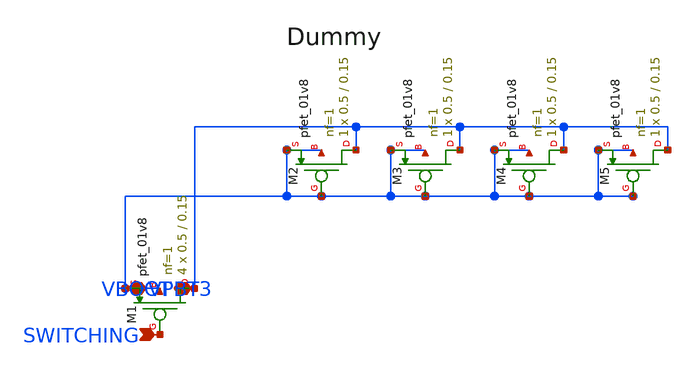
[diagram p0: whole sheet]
** sch_path: xschem/pcell_bsw_dischrg.sch
**.subckt pcell_bsw_dischrg VPBT3 SWITCHING VBOOT
*.iopin VPBT3
*.ipin SWITCHING
*.iopin VBOOT
XM1 VBOOT SWITCHING VPBT3 VPBT3 sky130_fd_pr__pfet_01v8 L=0.15 W=0.5 nf=1 ad='int((nf+1)/2) * W/nf * 0.29'
+ as='int((nf+2)/2) * W/nf * 0.29' pd='2*int((nf+1)/2) * (W/nf + 0.29)' ps='2*int((nf+2)/2) * (W/nf + 0.29)'
+ nrd='0.29 / W' nrs='0.29 / W' sa=0 sb=0 sd=0 mult=4 m=4
XM2 VBOOT VPBT3 VPBT3 VPBT3 sky130_fd_pr__pfet_01v8 L=0.15 W=0.5 nf=1 ad='int((nf+1)/2) * W/nf * 0.29'
+ as='int((nf+2)/2) * W/nf * 0.29' pd='2*int((nf+1)/2) * (W/nf + 0.29)' ps='2*int((nf+2)/2) * (W/nf + 0.29)'
+ nrd='0.29 / W' nrs='0.29 / W' sa=0 sb=0 sd=0 mult=1 m=1
XM3 VBOOT VPBT3 VPBT3 VPBT3 sky130_fd_pr__pfet_01v8 L=0.15 W=0.5 nf=1 ad='int((nf+1)/2) * W/nf * 0.29'
+ as='int((nf+2)/2) * W/nf * 0.29' pd='2*int((nf+1)/2) * (W/nf + 0.29)' ps='2*int((nf+2)/2) * (W/nf + 0.29)'
+ nrd='0.29 / W' nrs='0.29 / W' sa=0 sb=0 sd=0 mult=1 m=1
XM4 VBOOT VPBT3 VPBT3 VPBT3 sky130_fd_pr__pfet_01v8 L=0.15 W=0.5 nf=1 ad='int((nf+1)/2) * W/nf * 0.29'
+ as='int((nf+2)/2) * W/nf * 0.29' pd='2*int((nf+1)/2) * (W/nf + 0.29)' ps='2*int((nf+2)/2) * (W/nf + 0.29)'
+ nrd='0.29 / W' nrs='0.29 / W' sa=0 sb=0 sd=0 mult=1 m=1
XM5 VBOOT VPBT3 VPBT3 VPBT3 sky130_fd_pr__pfet_01v8 L=0.15 W=0.5 nf=1 ad='int((nf+1)/2) * W/nf * 0.29'
+ as='int((nf+2)/2) * W/nf * 0.29' pd='2*int((nf+1)/2) * (W/nf + 0.29)' ps='2*int((nf+2)/2) * (W/nf + 0.29)'
+ nrd='0.29 / W' nrs='0.29 / W' sa=0 sb=0 sd=0 mult=1 m=1
**.ends
.end
